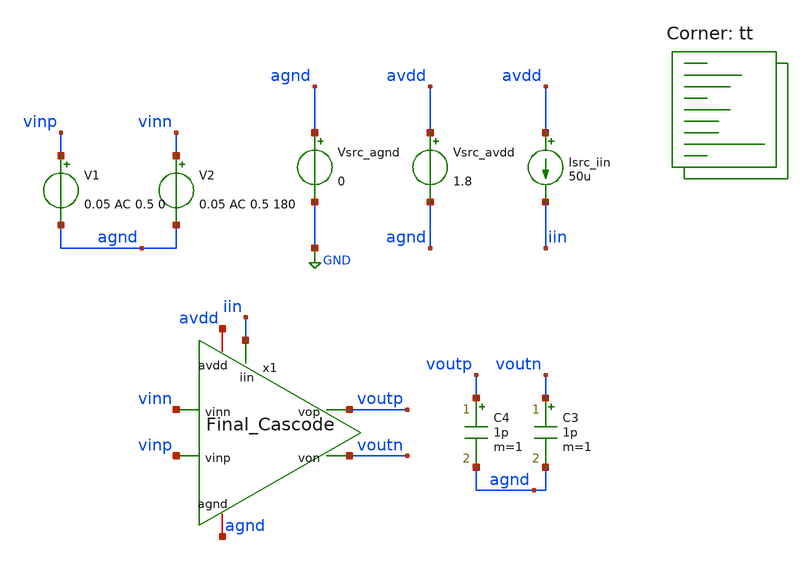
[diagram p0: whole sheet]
** sch_path: AMP/TB_Final_Cascode.sch
**.subckt TB_Final_Cascode
x1 avdd voutp voutn vinn vinp iin agnd Final_Cascode
Vsrc_agnd agnd GND 0
Vsrc_avdd avdd agnd 1.8
Isrc_iin avdd iin 50u
C3 voutn agnd 1p m=1
C4 voutp agnd 1p m=1
V1 vinp agnd 0.05 AC 0.5 0
V2 vinn agnd 0.05 AC 0.5 180
**** begin user architecture code

* this option enables mos model bin
* selection based on W/NF instead of W

.option savecurrents

.control
save all
op

* Print newline
echo

* Print stats for each MOSFET
foreach nmos x1.xm1 x1.xm2 x1.xm3 x1.xm4
 * Save stats
 save @m.{$nmos}.msky130_fd_pr__nfet_01v8[gm]
 let vth   = @m.{$nmos}.msky130_fd_pr__nfet_01v8[vth]
 let vgs   = @m.{$nmos}.msky130_fd_pr__nfet_01v8[vgs]
 let vds   = @m.{$nmos}.msky130_fd_pr__nfet_01v8[vds]
 let vdsat = @m.{$nmos}.msky130_fd_pr__nfet_01v8[vdsat]
 let gm    = @m.{$nmos}.msky130_fd_pr__nfet_01v8[gm]
 let gds   = @m.{$nmos}.msky130_fd_pr__nfet_01v8[gds]


 * Print stats
 echo Stats for $nmos:
 print vth
 print vgs
 print vds
 print vdsat
 print gm
 print gds

 * Print newline
 echo
end

foreach pmos x1.xm5 x1.xm6 x1.xm7 x1.xm8
 * Save stats
 save @m.{$pmos}.msky130_fd_pr__nfet_01v8[gm]
 let vth   = @m.{$pmos}.msky130_fd_pr__pfet_01v8[vth]
 let vgs   = @m.{$pmos}.msky130_fd_pr__pfet_01v8[vgs]
 let vds   = @m.{$pmos}.msky130_fd_pr__pfet_01v8[vds]
 let vdsat = @m.{$pmos}.msky130_fd_pr__pfet_01v8[vdsat]
 let gm    = @m.{$pmos}.msky130_fd_pr__pfet_01v8[gm]
 let gds   = @m.{$pmos}.msky130_fd_pr__pfet_01v8[gds]

 * Print stats
 echo Stats for $pmos:
 print vth
 print vgs
 print vds
 print vdsat
 print gm
 print gds

 * Print newline
 echo
end

* Print region of operation
echo Regions of Operation:
foreach nmos x1.xm1 x1.xm2 x1.xm3 x1.xm4
 * Save stats
 let vds = @m.{$nmos}.msky130_fd_pr__nfet_01v8[vds]
 let vgs = @m.{$nmos}.msky130_fd_pr__nfet_01v8[vgs]
 let vth = @m.{$nmos}.msky130_fd_pr__nfet_01v8[vth]

 * Check and print regions
 if (vgs <= vth)
  echo $nmos: N Cutoff
  print vgs
  print vth
 end
 if (vgs > vth) & (vds <= (vgs - vth))
  echo $nmos: N Triode
  print vgs
  print vth
  print vds
 end
 if (vgs > vth) & (vds > (vgs - vth))
  echo $nmos: N Saturation
 end
end

foreach pmos x1.xm5 x1.xm6 x1.xm7 x1.xm8
 * Save stats
 let vds = @m.{$pmos}.msky130_fd_pr__pfet_01v8[vds]
 let vgs = @m.{$pmos}.msky130_fd_pr__pfet_01v8[vgs]
 let vth = @m.{$pmos}.msky130_fd_pr__pfet_01v8[vth]

 * Check and print regions
 if (abs(vgs) <= abs(vth))
  echo $pmos: P Cutoff
  print vgs
  print vth
 end
 if (abs(vgs) > abs(vth)) & (abs(vds) <= (abs(vgs) - abs(vth)))
  echo $pmos: P Triode
  print vgs
  print vth
  print vds
 end
 if (abs(vgs) > abs(vth)) & (abs(vds) > (abs(vgs) - abs(vth)))
  echo $pmos: P Saturation
 end
end

* Print newline
echo

* Sweep frequency
write TB_Final_Cascode.raw
set appendwrite
ac dec 100 1 1e11
remzerovec

* Calculate gain
let vout_diff = v(voutp)- v(voutn)
let vin_diff = v(vinp)- v(vinn)
let gain = db(mag(vout_diff/vin_diff))
let ratio = (vout_diff/vin_diff)

write TB_Final_Cascode.raw

.endc


.lib $::SKYWATER_MODELS/sky130.lib.spice tt
**** end user architecture code
**.ends

* expanding   symbol:  /foss/designs/EE437/Project/ee437-quantum-controller/AMP/Final_Cascode.sym #
*+ of pins=7
** sym_path: AMP/Final_Cascode.sym
** sch_path: AMP/Final_Cascode.sch
.subckt Final_Cascode avdd vop von vinn vinp iin agnd
*.iopin avdd
*.ipin vinp
*.opin vop
*.iopin agnd
*.ipin vinn
*.opin von
*.ipin iin
XM1 int_n1 vinp itail agnd sky130_fd_pr__nfet_01v8 L=0.15 W=1 nf=1 ad='int((nf+1)/2) * W/nf * 0.29' as='int((nf+2)/2) * W/nf * 0.29'
+ pd='2*int((nf+1)/2) * (W/nf + 0.29)' ps='2*int((nf+2)/2) * (W/nf + 0.29)' nrd='0.29 / W' nrs='0.29 / W'
+ sa=0 sb=0 sd=0 mult=1 m=1
XM5 von Vb2 int_p1 agnd sky130_fd_pr__pfet_01v8 L=0.15 W=1 nf=1 ad='int((nf+1)/2) * W/nf * 0.29' as='int((nf+2)/2) * W/nf * 0.29'
+ pd='2*int((nf+1)/2) * (W/nf + 0.29)' ps='2*int((nf+2)/2) * (W/nf + 0.29)' nrd='0.29 / W' nrs='0.29 / W'
+ sa=0 sb=0 sd=0 mult=1 m=1
XM2 int_n2 vinn itail agnd sky130_fd_pr__nfet_01v8 L=0.15 W=1 nf=1 ad='int((nf+1)/2) * W/nf * 0.29' as='int((nf+2)/2) * W/nf * 0.29'
+ pd='2*int((nf+1)/2) * (W/nf + 0.29)' ps='2*int((nf+2)/2) * (W/nf + 0.29)' nrd='0.29 / W' nrs='0.29 / W'
+ sa=0 sb=0 sd=0 mult=1 m=1
XM3 von Vb1 int_n1 agnd sky130_fd_pr__nfet_01v8 L=0.15 W=1 nf=1 ad='int((nf+1)/2) * W/nf * 0.29' as='int((nf+2)/2) * W/nf * 0.29'
+ pd='2*int((nf+1)/2) * (W/nf + 0.29)' ps='2*int((nf+2)/2) * (W/nf + 0.29)' nrd='0.29 / W' nrs='0.29 / W'
+ sa=0 sb=0 sd=0 mult=1 m=1
XM4 vop Vb1 int_n2 agnd sky130_fd_pr__nfet_01v8 L=0.15 W=1 nf=1 ad='int((nf+1)/2) * W/nf * 0.29' as='int((nf+2)/2) * W/nf * 0.29'
+ pd='2*int((nf+1)/2) * (W/nf + 0.29)' ps='2*int((nf+2)/2) * (W/nf + 0.29)' nrd='0.29 / W' nrs='0.29 / W'
+ sa=0 sb=0 sd=0 mult=1 m=1
XM6 vop Vb2 int_p2 agnd sky130_fd_pr__pfet_01v8 L=0.15 W=1 nf=1 ad='int((nf+1)/2) * W/nf * 0.29' as='int((nf+2)/2) * W/nf * 0.29'
+ pd='2*int((nf+1)/2) * (W/nf + 0.29)' ps='2*int((nf+2)/2) * (W/nf + 0.29)' nrd='0.29 / W' nrs='0.29 / W'
+ sa=0 sb=0 sd=0 mult=1 m=1
XM7 int_p1 Vb3 avdd agnd sky130_fd_pr__pfet_01v8 L=0.15 W=1 nf=1 ad='int((nf+1)/2) * W/nf * 0.29' as='int((nf+2)/2) * W/nf * 0.29'
+ pd='2*int((nf+1)/2) * (W/nf + 0.29)' ps='2*int((nf+2)/2) * (W/nf + 0.29)' nrd='0.29 / W' nrs='0.29 / W'
+ sa=0 sb=0 sd=0 mult=1 m=1
XM8 int_p2 Vb3 avdd agnd sky130_fd_pr__pfet_01v8 L=0.15 W=1 nf=1 ad='int((nf+1)/2) * W/nf * 0.29' as='int((nf+2)/2) * W/nf * 0.29'
+ pd='2*int((nf+1)/2) * (W/nf + 0.29)' ps='2*int((nf+2)/2) * (W/nf + 0.29)' nrd='0.29 / W' nrs='0.29 / W'
+ sa=0 sb=0 sd=0 mult=1 m=1
XM9 iin iin agnd agnd sky130_fd_pr__nfet_01v8 L=0.15 W=1 nf=1 ad='int((nf+1)/2) * W/nf * 0.29' as='int((nf+2)/2) * W/nf * 0.29'
+ pd='2*int((nf+1)/2) * (W/nf + 0.29)' ps='2*int((nf+2)/2) * (W/nf + 0.29)' nrd='0.29 / W' nrs='0.29 / W'
+ sa=0 sb=0 sd=0 mult=1 m=1
XM10 itail iin agnd agnd sky130_fd_pr__nfet_01v8 L=0.15 W=1 nf=1 ad='int((nf+1)/2) * W/nf * 0.29' as='int((nf+2)/2) * W/nf * 0.29'
+ pd='2*int((nf+1)/2) * (W/nf + 0.29)' ps='2*int((nf+2)/2) * (W/nf + 0.29)' nrd='0.29 / W' nrs='0.29 / W'
+ sa=0 sb=0 sd=0 mult=1 m=1
Vsrc_Vb3_Ideal Vb3_Ideal agnd 1.35
Vsrc_Vb2_Ideal Vb2_Ideal agnd 1.15
Vsrc_Vb1_Ideal Vb1_Ideal agnd 0.95
Vsrc_Vb3 Vb3 Vb3_Ideal 0.0
Vsrc_Vb2 Vb2 Vb2_Ideal 0.0
Vsrc_Vb1 Vb1 Vb1_Ideal 0.0
.ends

.GLOBAL GND
.end
